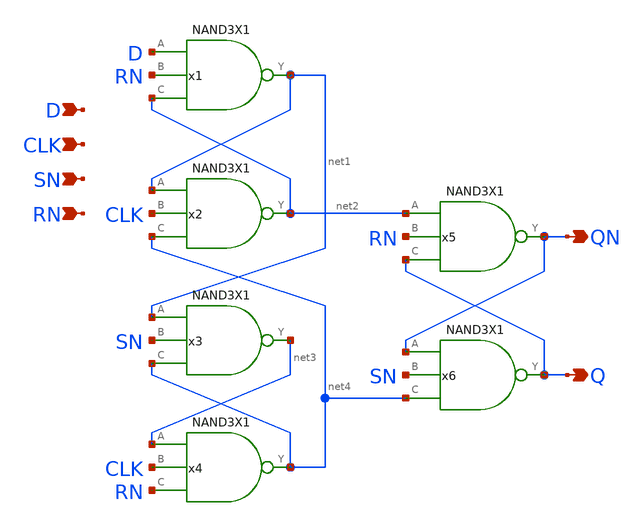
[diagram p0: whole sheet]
** sch_path: lib/xschem/DFFSNRNX1.sch
**.subckt DFFSNRNX1 Q QN D CLK SN RN
*.opin Q
*.opin QN
*.ipin D
*.ipin CLK
*.ipin SN
*.ipin RN
x3 net3 net1 SN net4 NAND3X1
x2 net2 net1 CLK net4 NAND3X1
x6 Q QN SN net4 NAND3X1
x1 net1 D RN net2 NAND3X1
x4 net4 net3 CLK RN NAND3X1
x5 QN net2 RN Q NAND3X1
**.ends

* expanding   symbol:  NAND3X1.sym # of pins=4
** sym_path: lib/xschem/NAND3X1.sym
** sch_path: lib/xschem/NAND3X1.sch
.subckt NAND3X1 Y A B C
*.opin Y
*.ipin A
*.ipin B
*.ipin C
XM1 net2 A VSS VSS sky130_fd_pr__nfet_01v8 L=0.15 W=3 nf=1 ad='int((nf+1)/2) * W/nf * 0.29' as='int((nf+2)/2) * W/nf * 0.29'
+ pd='2*int((nf+1)/2) * (W/nf + 0.29)' ps='2*int((nf+2)/2) * (W/nf + 0.29)' nrd='0.29 / W' nrs='0.29 / W'
+ sa=0 sb=0 sd=0 mult=1 m=1
XM2 Y A VDD VDD sky130_fd_pr__pfet_01v8 L=0.15 W=2 nf=1 ad='int((nf+1)/2) * W/nf * 0.29' as='int((nf+2)/2) * W/nf * 0.29'
+ pd='2*int((nf+1)/2) * (W/nf + 0.29)' ps='2*int((nf+2)/2) * (W/nf + 0.29)' nrd='0.29 / W' nrs='0.29 / W'
+ sa=0 sb=0 sd=0 mult=2 m=2
XM3 net1 B net2 VSS sky130_fd_pr__nfet_01v8 L=0.15 W=3 nf=1 ad='int((nf+1)/2) * W/nf * 0.29' as='int((nf+2)/2) * W/nf * 0.29'
+ pd='2*int((nf+1)/2) * (W/nf + 0.29)' ps='2*int((nf+2)/2) * (W/nf + 0.29)' nrd='0.29 / W' nrs='0.29 / W'
+ sa=0 sb=0 sd=0 mult=1 m=1
XM4 Y C net1 VSS sky130_fd_pr__nfet_01v8 L=0.15 W=3 nf=1 ad='int((nf+1)/2) * W/nf * 0.29' as='int((nf+2)/2) * W/nf * 0.29'
+ pd='2*int((nf+1)/2) * (W/nf + 0.29)' ps='2*int((nf+2)/2) * (W/nf + 0.29)' nrd='0.29 / W' nrs='0.29 / W'
+ sa=0 sb=0 sd=0 mult=1 m=1
XM6 Y B VDD VDD sky130_fd_pr__pfet_01v8 L=0.15 W=2 nf=1 ad='int((nf+1)/2) * W/nf * 0.29' as='int((nf+2)/2) * W/nf * 0.29'
+ pd='2*int((nf+1)/2) * (W/nf + 0.29)' ps='2*int((nf+2)/2) * (W/nf + 0.29)' nrd='0.29 / W' nrs='0.29 / W'
+ sa=0 sb=0 sd=0 mult=2 m=2
XM8 Y C VDD VDD sky130_fd_pr__pfet_01v8 L=0.15 W=2 nf=1 ad='int((nf+1)/2) * W/nf * 0.29' as='int((nf+2)/2) * W/nf * 0.29'
+ pd='2*int((nf+1)/2) * (W/nf + 0.29)' ps='2*int((nf+2)/2) * (W/nf + 0.29)' nrd='0.29 / W' nrs='0.29 / W'
+ sa=0 sb=0 sd=0 mult=2 m=2
.ends

.end
